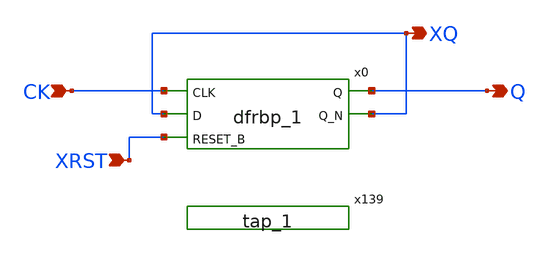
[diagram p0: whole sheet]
** sch_path: design/schematic/TFF.sch
**.subckt TFF CK XRST XQ Q
*.ipin CK
*.ipin XRST
*.opin XQ
*.opin Q
x0 CK XQ XRST GND GND DVDD DVDD Q XQ sky130_fd_sc_hd__dfrbp_1
x139 GND GND DVDD DVDD sky130_fd_sc_hd__tap_1
**.ends
.end
